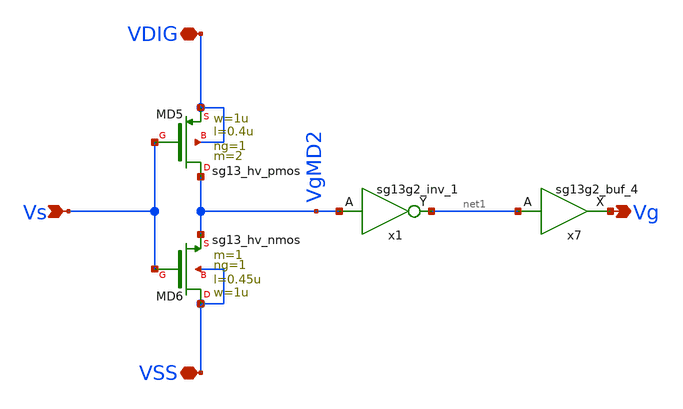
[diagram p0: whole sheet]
** sch_path: AC3E_USM_TDBUCK/design_data/xschem/LSHL/LSHL_vto1p1.sch
* IHP-GmbH/IHP-Open-PDK/ihp-sg13g2/libs.tech/xschem/sg13g2_stdcells/sg13g2_buf_4.sch:
* Copyright 2023 IHP PDK Authors
* Licensed under the Apache License, Version 2.0 (the "License");
**.subckt LSHL_vto1p1 VDIG Vs Vg VSS
*.iopin VDIG
*.ipin Vs
*.opin Vg
*.iopin VSS
XMD5 VgMD2 Vs VDIG VDIG sg13_hv_pmos w=1u l=0.4u ng=1 m=2 mm_ok=1
XMD6 VSS Vs VgMD2 VSS sg13_hv_nmos w=1u l=0.45u ng=1 m=1 mm_ok=1
x7 Vg net1 VDIG VSS sg13g2_buf_4
x1 net1 VgMD2 VDIG VSS sg13g2_inv_1
**.ends

* expanding   symbol:  sg13g2_stdcells/sg13g2_buf_4.sym # of pins=2
** sym_path: sg13g2_stdcells/sg13g2_buf_4.sym
** sch_path: sg13g2_stdcells/sg13g2_buf_4.sch
.subckt sg13g2_buf_4 X A VDD VSS
*.ipin A
*.opin X
*.iopin VDD
*.iopin VSS
XM1 net1 A VSS VSS sg13_lv_nmos w=740.00n l=130.00n ng=1 m=1 mm_ok=1
XM2 X net1 VSS VSS sg13_lv_nmos w=2.96u l=130.00n ng=4 m=1 mm_ok=1
XM3 net1 A VDD VDD sg13_lv_pmos w=1.68u l=130.00n ng=2 m=1 mm_ok=1
XM4 X net1 VDD VDD sg13_lv_pmos w=4.48u l=130.00n ng=4 m=1 mm_ok=1
.ends


* expanding   symbol:  sg13g2_stdcells/sg13g2_inv_1.sym # of pins=2
** sym_path: sg13g2_stdcells/sg13g2_inv_1.sym
** sch_path: sg13g2_stdcells/sg13g2_inv_1.sch
.subckt sg13g2_inv_1 Y A VDD VSS
*.opin Y
*.ipin A
*.iopin VDD
*.iopin VSS
XM1 Y A VSS VSS sg13_lv_nmos w=740.00n l=130.00n ng=1 m=1 mm_ok=1
XM2 Y A VDD VDD sg13_lv_pmos w=1.12u l=130.00n ng=1 m=1 mm_ok=1
.ends

.end
